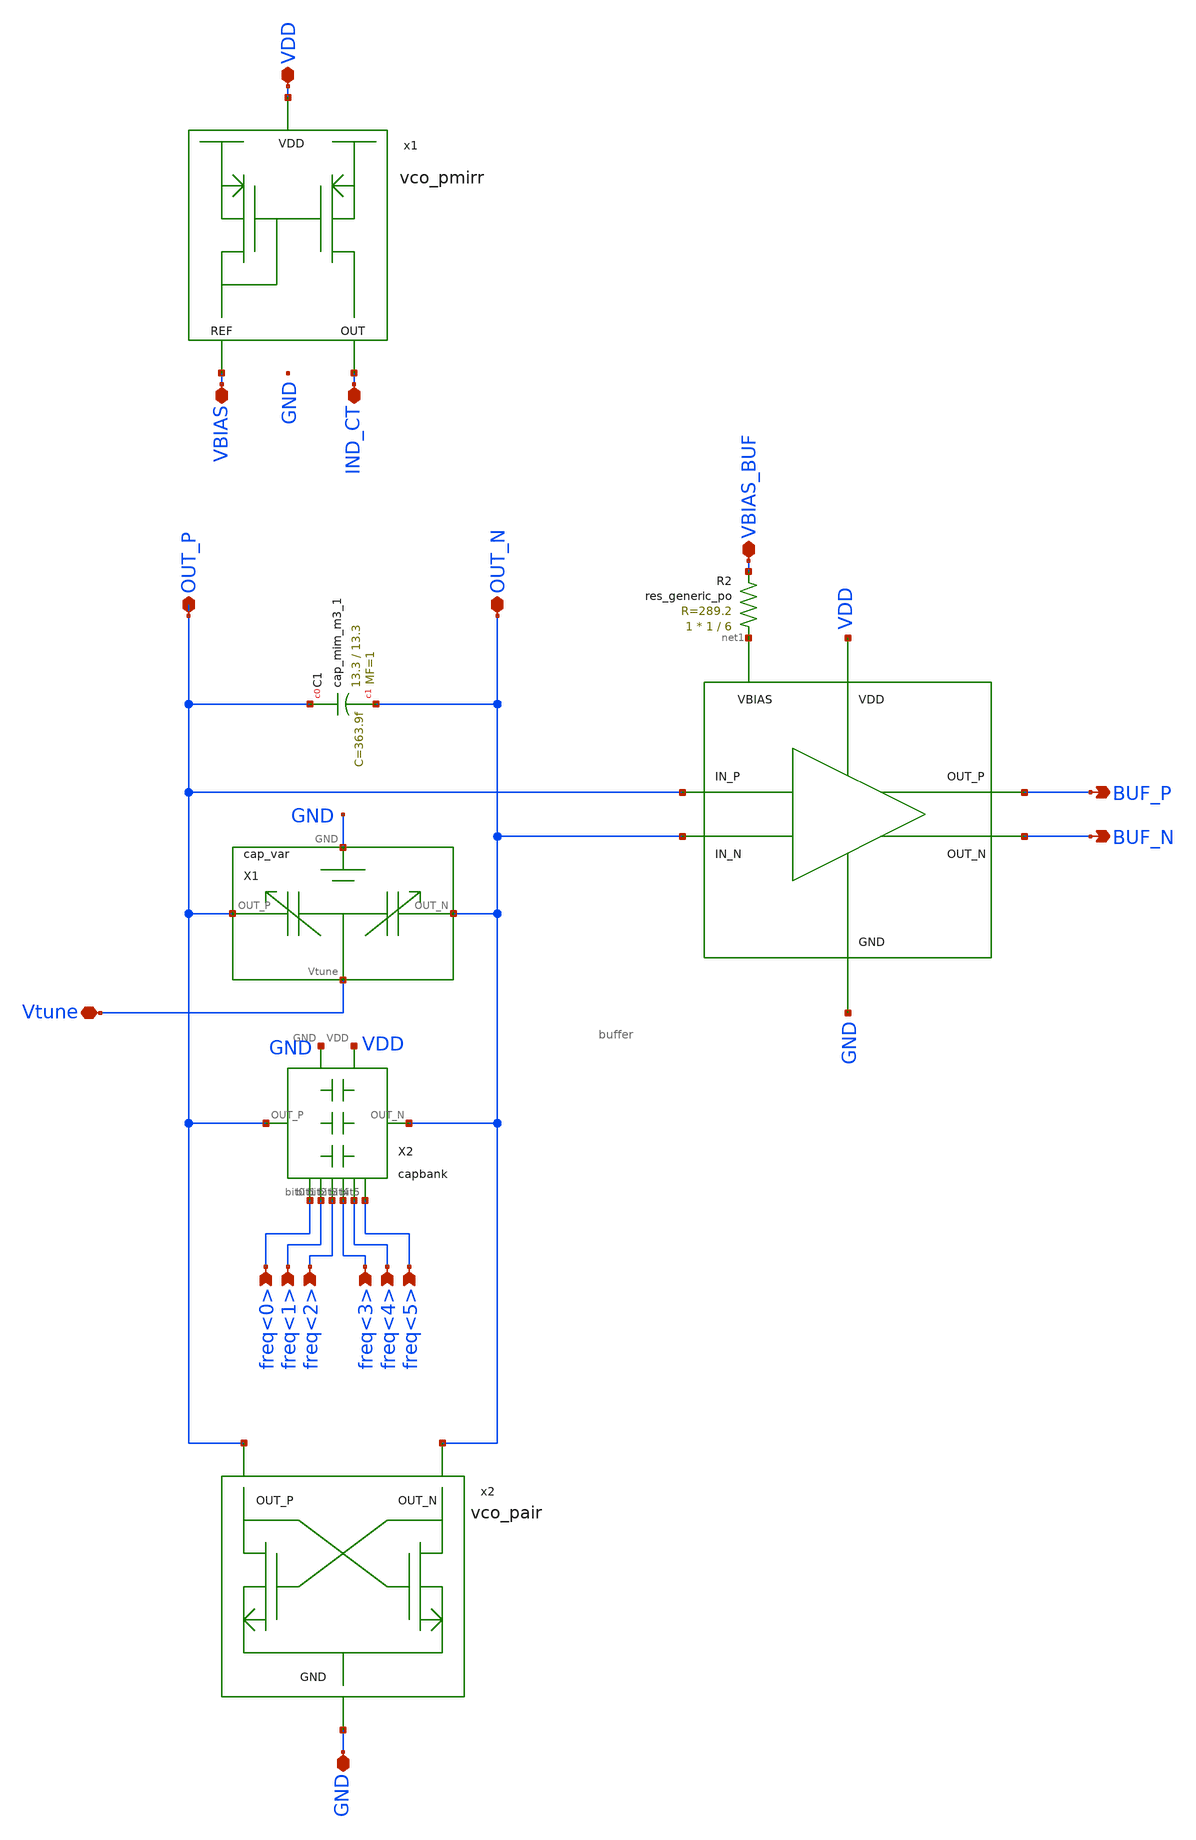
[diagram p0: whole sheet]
** sch_path: xschem/vco_wo_ind.sch
**.subckt vco_wo_ind OUT_P IND_CT Vtune freq<0> freq<1> freq<2> freq<3> freq<4> freq<5> GND BUF_P
*+ BUF_N OUT_N VBIAS_BUF VDD VBIAS
*.iopin OUT_P
*.iopin IND_CT
*.iopin Vtune
*.ipin freq<0>
*.ipin freq<1>
*.ipin freq<2>
*.ipin freq<3>
*.ipin freq<4>
*.ipin freq<5>
*.iopin GND
*.opin BUF_P
*.opin BUF_N
*.iopin OUT_N
*.iopin VBIAS_BUF
*.iopin VDD
*.iopin VBIAS
X1 OUT_P OUT_N GND Vtune cap_var
X2 OUT_P OUT_N VDD GND freq<0> freq<1> freq<2> freq<3> freq<4> freq<5> capbank
XC1 OUT_P OUT_N sky130_fd_pr__cap_mim_m3_1 W=13.3 L=13.3 MF=1 m=1
XR2 net1 VBIAS_BUF sky130_fd_pr__res_generic_po W=1 L=6 m=1
x1 VDD IND_CT VBIAS vco_pmirr
x2 OUT_P OUT_N GND vco_pair
X3 net1 VDD GND BUF_N BUF_P OUT_P OUT_N buffer
**.ends
.end
